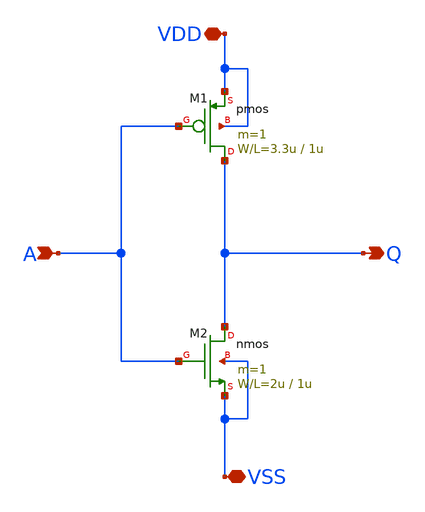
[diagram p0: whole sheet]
** sch_path: member_project/sanken/yukiyama/inverter1.sch
**.subckt inverter1 A Q VDD VSS
*.ipin A
*.opin Q
*.iopin VDD
*.iopin VSS
M1 Q A VDD VDD pmos L=1u W=3.3u m=1
M2 Q A VSS VSS nmos L=1u W=2u m=1
**.ends
.end
